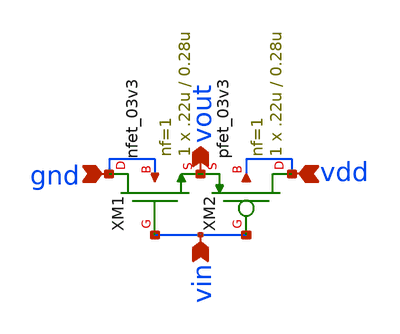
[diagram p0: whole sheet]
** sch_path: SAR_ADC/xschem/spice/symbols/inv.sch
**.subckt inv gnd vdd vin vout
*.ipin gnd
*.ipin vdd
*.ipin vin
*.opin vout
XM1 gnd vin vout gnd nfet_03v3 L=0.28u W=.22u nf=1 ad='int((nf+1)/2) * W/nf * 0.18u' as='int((nf+2)/2) * W/nf * 0.18u'
+ pd='2*int((nf+1)/2) * (W/nf + 0.18u)' ps='2*int((nf+2)/2) * (W/nf + 0.18u)' nrd='0.18u / W' nrs='0.18u / W'
+ sa=0 sb=0 sd=0 m=1
XM2 vdd vin vout vdd pfet_03v3 L=0.28u W=.22u nf=1 ad='int((nf+1)/2) * W/nf * 0.18u' as='int((nf+2)/2) * W/nf * 0.18u'
+ pd='2*int((nf+1)/2) * (W/nf + 0.18u)' ps='2*int((nf+2)/2) * (W/nf + 0.18u)' nrd='0.18u / W' nrs='0.18u / W'
+ sa=0 sb=0 sd=0 m=1
**.ends
.end
